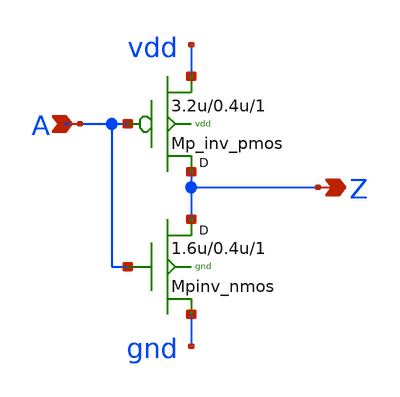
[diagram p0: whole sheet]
** sch_path: sram_4_16_scn4m/pinv_6.sch
**.subckt pinv_6 A Z
*.ipin A
*.opin Z
Mpinv_nmos Z A gnd gnd n w=1.6u l=0.4u m=1
Mp_inv_pmos Z A vdd vdd p w=3.2u l=0.4u m=1
**.ends
.end
